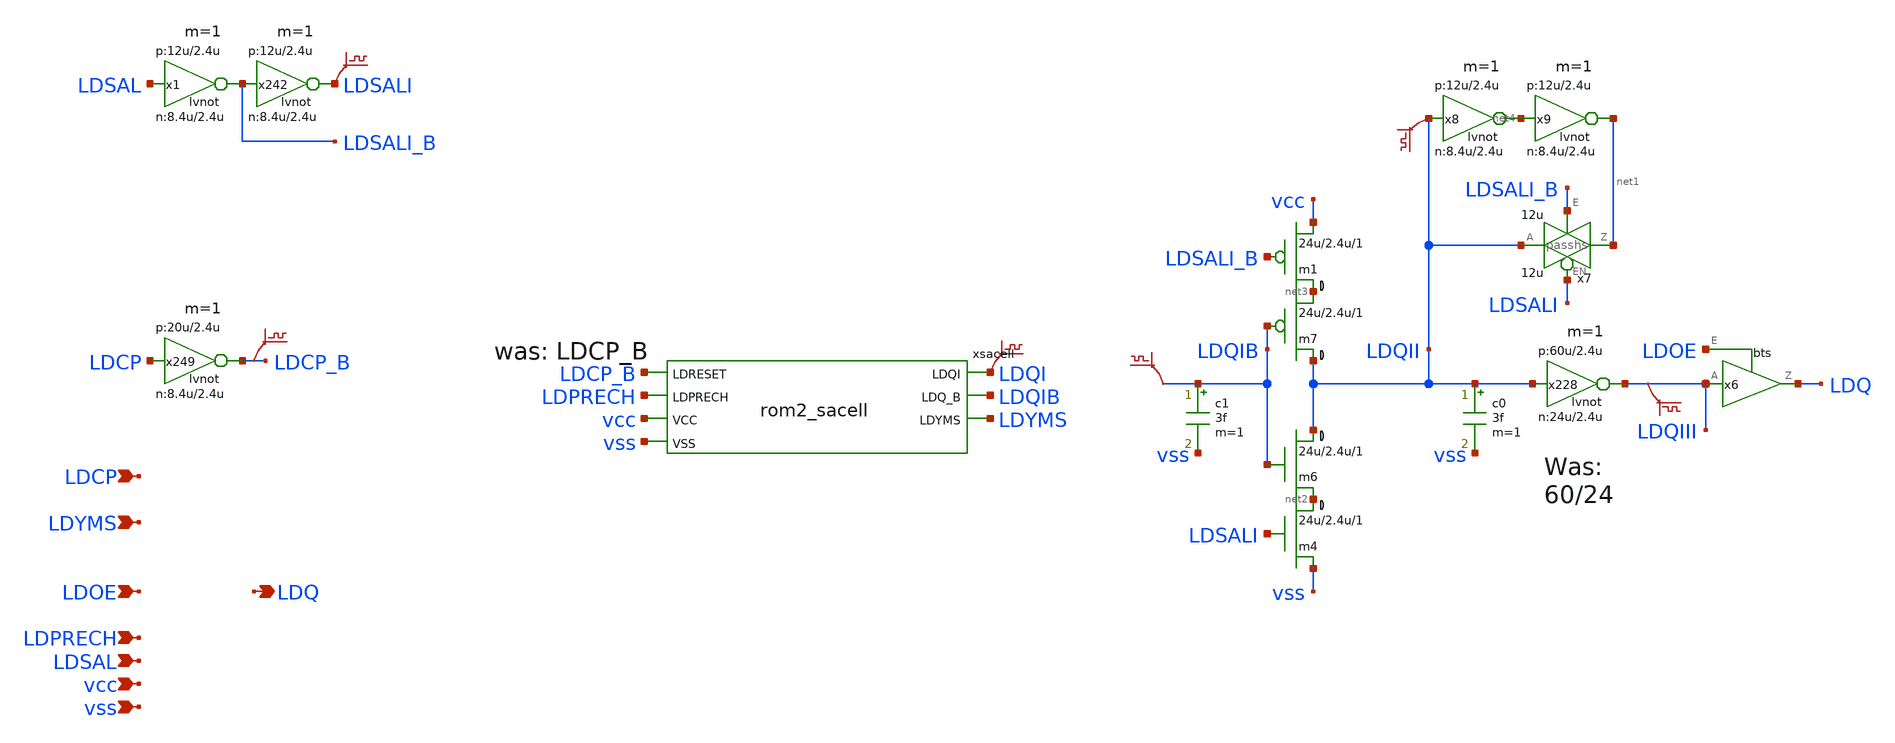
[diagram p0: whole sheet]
** sch_path: xschem-src/xschem_library/rom8k/rom2_sa.sch
* Copyright (C) 1998-2026 Stefan Frederik Schippers
* This program is free software; you can redistribute it and/or modify
* it under the terms of the GNU General Public License as published by
* the Free Software Foundation; either version 2 of the License, or
* (at your option) any later version.
* This program is distributed in the hope that it will be useful,
* but WITHOUT ANY WARRANTY; without even the implied warranty of
* MERCHANTABILITY or FITNESS FOR A PARTICULAR PURPOSE.  See the
* GNU General Public License for more details.
* You should have received a copy of the GNU General Public License
* along with this program; if not, write to the Free Software
**.subckt rom2_sa LDQ LDCP LDYMS LDOE LDPRECH LDSAL vcc vss
*.opin LDQ
*.ipin LDCP
*.ipin LDYMS
*.ipin LDOE
*.ipin LDPRECH
*.ipin LDSAL
*.ipin vcc
*.ipin vss
x242 LDSALI LDSALI_B vcc vss lvnot wn=8.4u lln=2.4u wp=12u lp=2.4u m=1
x249 LDCP_B LDCP vcc vss lvnot wn=8.4u lln=2.4u wp=20u lp=2.4u m=1
x6 LDQ LDQIII LDOE vcc vss bts
x7 net1 LDQII LDSALI LDSALI_B vcc vss passhs WN=12u LN=1.2u WP=12u LP=1.2u
m6 LDQII LDQIB net2 0 cmosn w=24u l=2.4u ad={24u *4.4u} as={24u *4.4u} pd={24u *2 + 8.8u} ps={24u *2 + 8.8u}
+ m=1
m7 LDQII LDQIB net3 VCC cmosp w=24u l=2.4u ad={24u *4.4u} as={24u *4.4u} pd={24u *2 + 8.8u} ps={24u *2 + 8.8u}
+ m=1
m4 net2 LDSALI vss 0 cmosn w=24u l=2.4u ad={24u *4.4u} as={24u *4.4u} pd={24u *2 + 8.8u} ps={24u *2 + 8.8u}
+ m=1
m1 net3 LDSALI_B vcc VCC cmosp w=24u l=2.4u ad={24u *4.4u} as={24u *4.4u} pd={24u *2 + 8.8u} ps={24u *2 + 8.8u}
+ m=1
x8 net4 LDQII vcc vss lvnot wn=8.4u lln=2.4u wp=12u lp=2.4u m=1
x9 net1 net4 vcc vss lvnot wn=8.4u lln=2.4u wp=12u lp=2.4u m=1
c0 LDQII vss 3f m=1
c1 LDQIB vss 3f m=1
x228 LDQIII LDQII vcc vss lvnot wn=24u lln=2.4u wp=60u lp=2.4u m=1
x1 LDSALI_B LDSAL vcc vss lvnot wn=8.4u lln=2.4u wp=12u lp=2.4u m=1
xsacell LDCP_B LDPRECH vcc vss LDQI LDQIB LDYMS rom2_sacell
.save v(ldqib)
.save v(ldqii)
.save v(ldcp_b)
.save v(ldsali)
.save v(ldqi)
.save v(ldqiii)
**.ends

* expanding   symbol:  lvnot.sym # of pins=2
** sym_path: xschem-src/xschem_library/rom8k/lvnot.sym
** sch_path: xschem-src/xschem_library/rom8k/lvnot.sch
.subckt lvnot y a VCCPIN VSSPIN     wn=10u lln=1.2u wp=10u lp=1.2u
*.opin y
*.ipin a
m2 DP a VCCPIN VCCPIN cmosp w=wp l=lp ad='wp *4.6u' as='wp *4.6u' pd='wp *2+9.2u' ps='wp *2+9.2u' m=1
m1 DN a VSSPIN VSSPIN cmosn w=wn l=lln ad='wn *4.3u' as='wn *4.3u' pd='wn *2+8.6u' ps='wn *2+8.6u' m=1
Vmeas DP y 0
.save i(vmeas)
Vmeas1 y DN 0
.save i(vmeas1)
.save v(dp)
.save v(dn)
.ends


* expanding   symbol:  bts.sym # of pins=3
** sym_path: xschem-src/xschem_library/rom8k/bts.sym
** sch_path: xschem-src/xschem_library/rom8k/bts.sch
.subckt bts Z A E VCCPIN VSSPIN
*.ipin A
*.ipin E
*.opin Z
m7 NN EN PP VCCPIN cmosp w=56u l=2.4u ad={56u *2.2u} as={56u *2.2u} pd={56u *2+4.4u} ps={56u *2+4.4u}
+ m=1
m8 PP A VCCPIN VCCPIN cmosp w=56u l=2.4u ad={56u *2.2u} as={56u *2.2u} pd={56u *2+4.4u} ps={56u *2+4.4u}
+ m=1
m9 NN A VSSPIN 0 cmosn w=20u l=2.4u ad={20u *4.4u} as={20u *4.4u} pd={20u *2 + 8.8u} ps={20u *2 + 8.8u}
+ m=1
m1 PP E NN 0 cmosn w=24u l=2.4u ad={24u *4.4u} as={24u *4.4u} pd={24u *2 + 8.8u} ps={24u *2 + 8.8u} m=1
m11 Z PP VCCPIN VCCPIN cmosp w=200u l=2.4u ad={200u *2.2u} as={200u *2.2u} pd={200u *2+4.4u} ps={200u *2+4.4u}
+ m=1
m12 Z NN VSSPIN 0 cmosn w=80u l=2.4u ad={80u *4.4u} as={80u *4.4u} pd={80u *2 + 8.8u} ps={80u *2 + 8.8u}
+ m=1
m13 NN EN VSSPIN 0 cmosn w=20u l=2.4u ad={20u *4.4u} as={20u *4.4u} pd={20u *2 + 8.8u} ps={20u *2 + 8.8u}
+ m=1
m14 PP E VCCPIN VCCPIN cmosp w=50u l=2.4u ad={50u *2.2u} as={50u *2.2u} pd={50u *2+4.4u} ps={50u *2+4.4u}
+ m=1
m15 EN E VCCPIN VCCPIN cmosp w=50u l=2.4u ad={50u *2.2u} as={50u *2.2u} pd={50u *2+4.4u} ps={50u *2+4.4u}
+ m=1
m16 EN E VSSPIN 0 cmosn w=20u l=2.4u ad={20u *4.4u} as={20u *4.4u} pd={20u *2 + 8.8u} ps={20u *2 + 8.8u}
+ m=1
c0 E VSSPIN 3f m=1
c4 NN VSSPIN 3f m=1
c5 PP VSSPIN 3f m=1
c6 EN VSSPIN 3f m=1
.ends


* expanding   symbol:  passhs.sym # of pins=4
** sym_path: xschem-src/xschem_library/rom8k/passhs.sym
** sch_path: xschem-src/xschem_library/rom8k/passhs.sch
.subckt passhs Z A EN E VCCPIN VSSPIN  WN=2u LN=1.2u WP=2u LP=1.2u
*.iopin Z
*.iopin A
*.ipin EN
*.ipin E
m60 Z EN A VCCPIN cmosp w=WP l=2.4u ad='WP *4.6u' as='WP *4.6u' pd='WP *2+9.2u' ps='WP *2+9.2u' m=1
m1 A E Z VSSPIN cmosn w=WN l=2.4u ad='WN *4.3u' as='WN *4.3u' pd='WN *2+8.6u' ps='WN *2+8.6u' m=1
* noconn VSSPIN
* noconn VCCPIN
.ends


* expanding   symbol:  rom2_sacell.sym # of pins=7
** sym_path: xschem-src/xschem_library/rom8k/rom2_sacell.sym
** sch_path: xschem-src/xschem_library/rom8k/rom2_sacell.sch
.subckt rom2_sacell LDRESET LDPRECH VCC VSS LDQI LDQ_B LDYMS
*.ipin LDRESET
*.ipin LDPRECH
*.ipin VCC
*.ipin VSS
*.opin LDQI
*.opin LDQ_B
*.iopin LDYMS
m3 VCC LDPRECH LDYMS VSS cmosn w=WPRECH l=2u ad='WPRECH *4.3u' as='WPRECH *4.3u' pd='WPRECH *2+8.6u'
+ ps='WPRECH *2+8.6u' m=10
m1 LDQI VCC LDYMS VSS cmosn w=WPRECH l=2u ad='WPRECH *4.3u' as='WPRECH *4.3u' pd='WPRECH *2+8.6u' ps='WPRECH *2+8.6u'
+ m=2
m5 LDQI LDRESET VCC VCC cmosp w=6.6u l=8.8u ad={6.6u *4.4u} as={6.6u *4.4u} pd={6.6u *2 + 8.8u} ps={6.6u *2 + 8.8u}
+ m=1
m11 LDYMS LDRESET VSS 0 cmosn w=16u l=2.4u ad={16u *4.4u} as={16u *4.4u} pd={16u *2 + 8.8u} ps={16u *2 + 8.8u}
+ m=1
c2 LDQI VSS 3f m=1
m2 LDQ_B LDQI VSS 0 cmosn w=8u l=2.4u ad={8u *4.4u} as={8u *4.4u} pd={8u *2 + 8.8u} ps={8u *2 + 8.8u}
+ m=1
m4 LDQ_B LDQI VCC VCC cmosp w=40u l=2.4u ad='40u *4.6u' as='40u *4.6u' pd='40u *2+9.2u' ps='40u *2+9.2u'
+ m=1
.ends

.end
